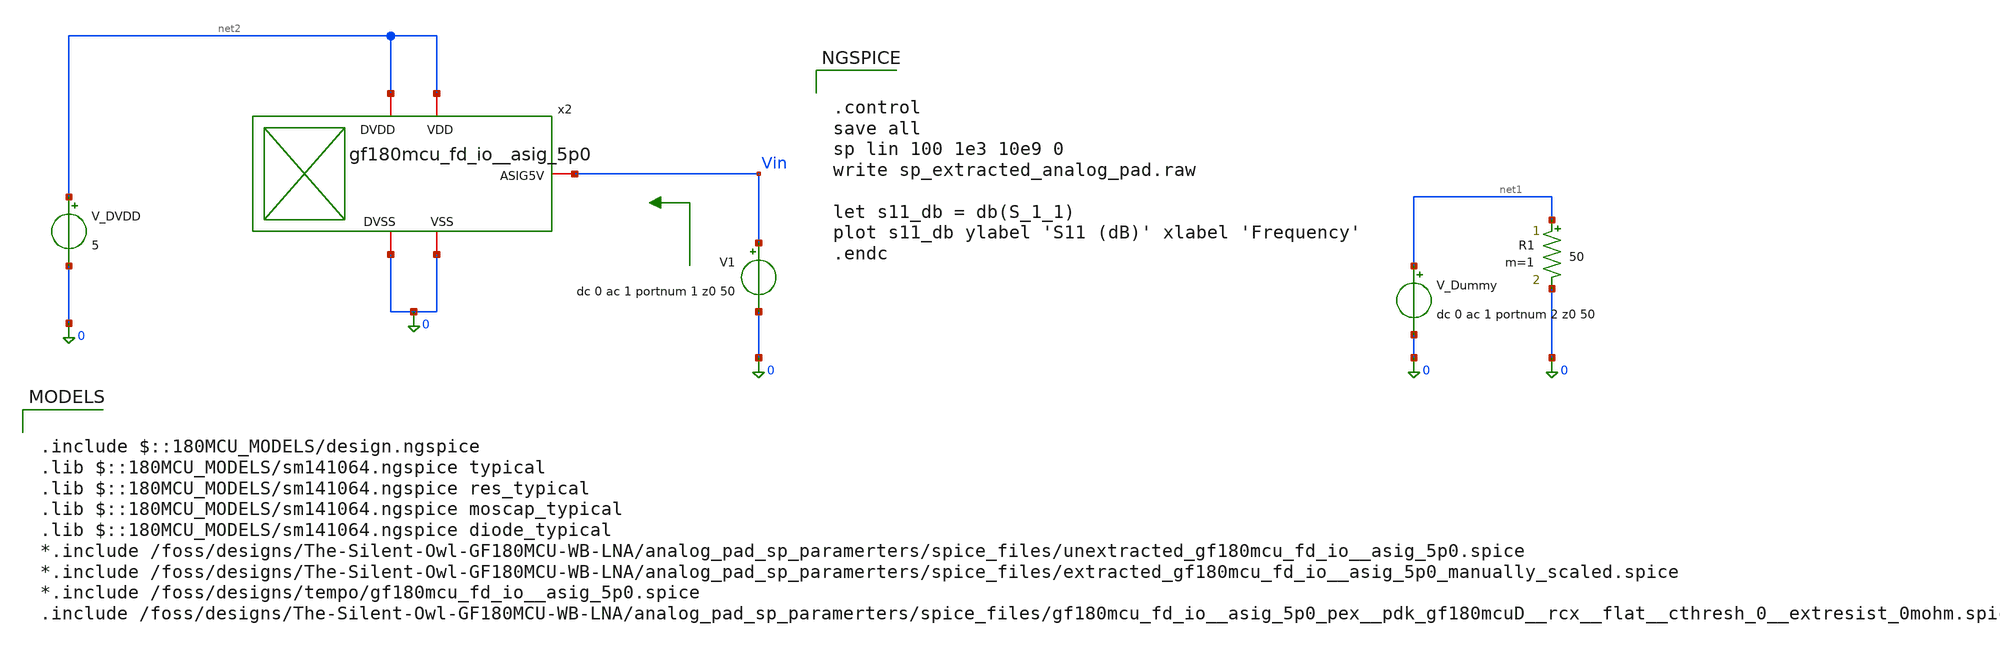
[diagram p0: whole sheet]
** sch_path: analog_pad_sp_paramerters/xschem/schematic_extracted_sp.sch
**.subckt schematic_extracted_sp
V1 Vin 0 dc 0 ac 1 portnum 1 z0 50
V_DVDD net2 0 5
V_Dummy net1 0 dc 0 ac 1 portnum 2 z0 50
R1 net1 0 50 m=1
x2 Vin net2 0 net2 0 gf180mcu_fd_io__asig_5p0
**** begin user architecture code


.control
save all
sp lin 100 1e3 10e9 0
write sp_extracted_analog_pad.raw

let s11_db = db(S_1_1)
plot s11_db ylabel 'S11 (dB)' xlabel 'Frequency'
.endc



.include $::180MCU_MODELS/design.ngspice
.lib $::180MCU_MODELS/sm141064.ngspice typical
.lib $::180MCU_MODELS/sm141064.ngspice res_typical
.lib $::180MCU_MODELS/sm141064.ngspice moscap_typical
.lib $::180MCU_MODELS/sm141064.ngspice diode_typical
*.include /foss/designs/The-Silent-Owl-GF180MCU-WB-LNA/analog_pad_sp_paramerters/spice_files/unextracted_gf180mcu_fd_io__asig_5p0.spice
*.include /foss/designs/The-Silent-Owl-GF180MCU-WB-LNA/analog_pad_sp_paramerters/spice_files/extracted_gf180mcu_fd_io__asig_5p0_manually_scaled.spice
*.include /foss/designs/tempo/gf180mcu_fd_io__asig_5p0.spice
.include /foss/designs/The-Silent-Owl-GF180MCU-WB-LNA/analog_pad_sp_paramerters/spice_files/gf180mcu_fd_io__asig_5p0_pex__pdk_gf180mcuD__rcx__flat__cthresh_0__extresist_0mohm.spice

**** end user architecture code
**.ends
.end
